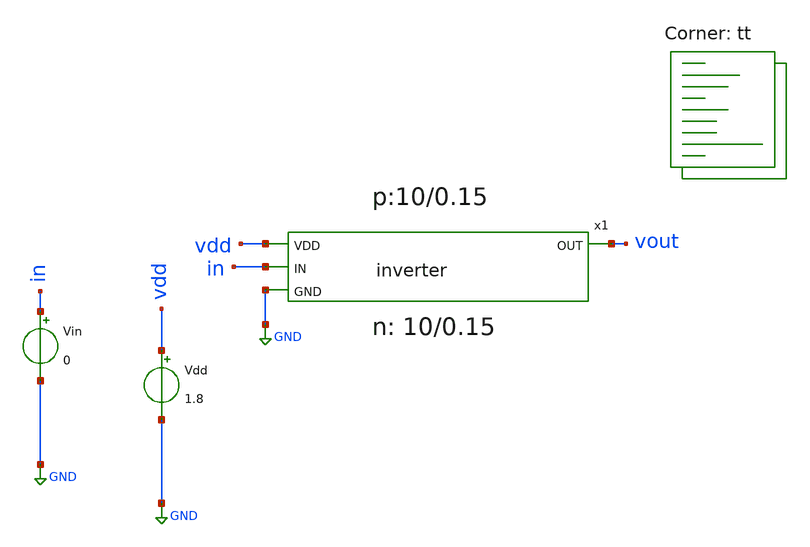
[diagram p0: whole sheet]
** sch_path: tb_inverter.sch
**.subckt tb_inverter
Vin in GND 0
Vdd vdd GND 1.8
x1 vdd vout in GND inverter
**** begin user architecture code



.options savecurrents


.param pmos_width=10

.control
save all
dc vin 0 1.8 1m
plot v(v-sweep) v(vout)

.endc


.lib $::SKYWATER_MODELS/sky130.lib.spice tt
**** end user architecture code
**.ends

* expanding   symbol:  inverter.sym # of pins=4
** sym_path: inverter.sym
** sch_path: inverter.sch
.subckt inverter VDD OUT IN GND
*.ipin IN
*.ipin VDD
*.opin OUT
*.ipin GND
XM2 OUT IN GND GND sky130_fd_pr__nfet_01v8 L=0.15 W=20 nf=1 ad='int((nf+1)/2) * W/nf * 0.29' as='int((nf+2)/2) * W/nf * 0.29'
+ pd='2*int((nf+1)/2) * (W/nf + 0.29)' ps='2*int((nf+2)/2) * (W/nf + 0.29)' nrd='0.29 / W' nrs='0.29 / W'
+ sa=0 sb=0 sd=0 mult=1 m=1
XM1 OUT IN VDD VDD sky130_fd_pr__pfet_01v8 L=0.15 W=56 nf=1 ad='int((nf+1)/2) * W/nf * 0.29' as='int((nf+2)/2) * W/nf * 0.29'
+ pd='2*int((nf+1)/2) * (W/nf + 0.29)' ps='2*int((nf+2)/2) * (W/nf + 0.29)' nrd='0.29 / W' nrs='0.29 / W'
+ sa=0 sb=0 sd=0 mult=1 m=1
.ends

.GLOBAL GND
.end
